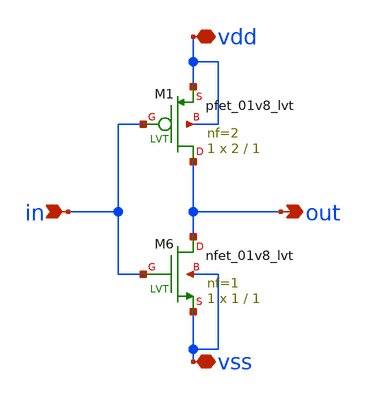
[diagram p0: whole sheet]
** sch_path: BGR_TOP_SKY130A/NOT.sch
**.subckt NOT vdd vss in out
*.iopin vdd
*.iopin vss
*.ipin in
*.opin out
XM6 out in vss vss sky130_fd_pr__nfet_01v8_lvt L=1 W=1 nf=1 ad='int((1 + 1)/2) * 1 / 1 * 0.29' as='int((1 + 2)/2) * 1 / 1 * 0.29'
+ pd='2*int((1 + 1)/2) * (1 / 1 + 0.29)' ps='2*int((1 + 2)/2) * (1 / 1 + 0.29)' nrd='0.29 / 1 ' nrs='0.29 / 1 '
+ sa=0 sb=0 sd=0 mult=1 m=1
XM1 out in vdd vdd sky130_fd_pr__pfet_01v8_lvt L=1 W=2 nf=2 ad='int((2 + 1)/2) * 2 / 2 * 0.29' as='int((2 + 2)/2) * 2 / 2 * 0.29'
+ pd='2*int((2 + 1)/2) * (2 / 2 + 0.29)' ps='2*int((2 + 2)/2) * (2 / 2 + 0.29)' nrd='0.29 / 2 ' nrs='0.29 / 2 '
+ sa=0 sb=0 sd=0 mult=1 m=1
**.ends
.end
